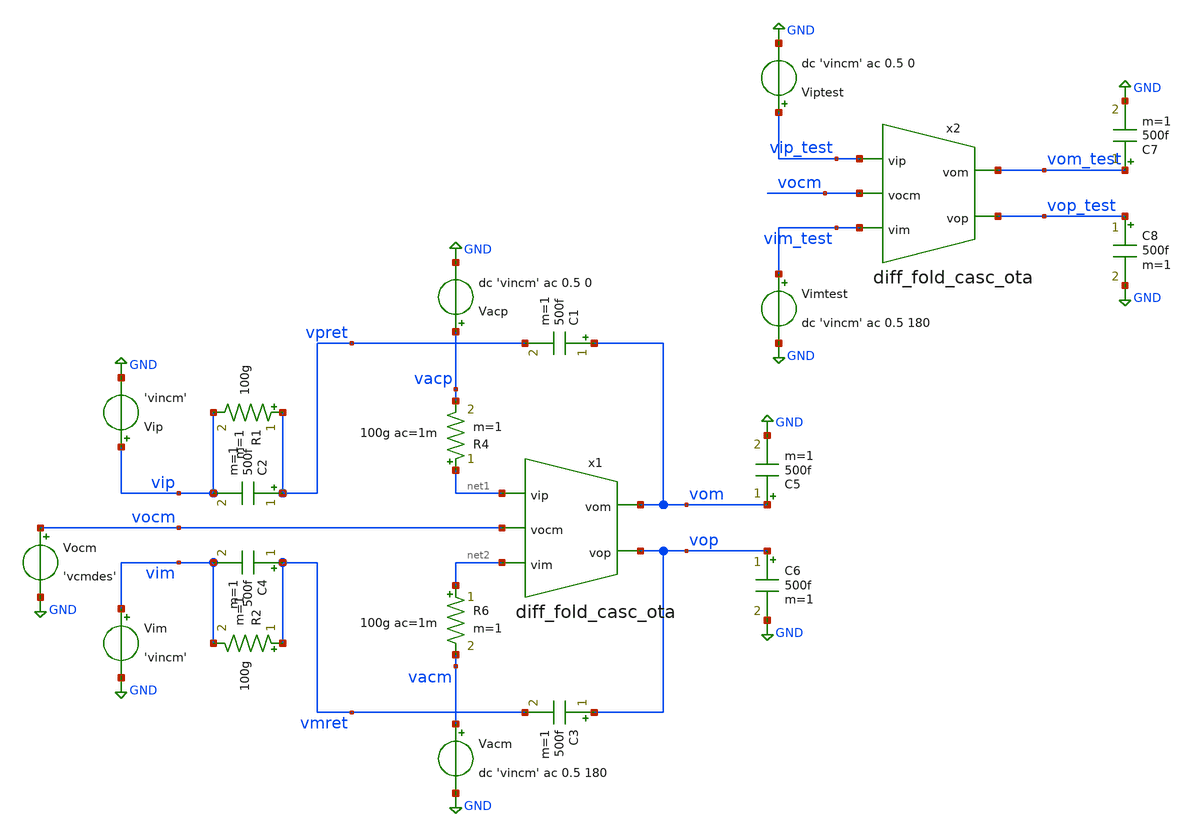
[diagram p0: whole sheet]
** sch_path: designs/diff_ota_stability_tb.sch
* Copyright 2020 Stefan Frederik Schippers
* Licensed under the Apache License, Version 2.0 (the "License");
* you may not use this file except in compliance with the License.
* You may obtain a copy of the License at
* https://www.apache.org/licenses/LICENSE-2.0
* Unless required by applicable law or agreed to in writing, software
* distributed under the License is distributed on an "AS IS" BASIS,
* WITHOUT WARRANTIES OR CONDITIONS OF ANY KIND, either express or implied.
* See the License for the specific language governing permissions and
* limitations under the License.
**.subckt diff_ota_stability_tb
C1 vom vpret 500f m=1
C2 vpret vip 500f m=1
C3 vop vmret 500f m=1
C4 vmret vim 500f m=1
C5 vom GND 500f m=1
C6 vop GND 500f m=1
R1 vpret vip 100g m=1
R2 vmret vim 100g m=1
R4 net1 vacp 100g ac=1m m=1
R6 net2 vacm 100g ac=1m m=1
Vacm vacm GND dc 'vincm' ac 0.5 180
Vacp vacp GND dc 'vincm' ac 0.5 0
Vip vip GND 'vincm'
Vim vim GND 'vincm'
Vocm vocm GND 'vcmdes'
Viptest vip_test GND dc 'vincm' ac 0.5 0
Vimtest vim_test GND dc 'vincm' ac 0.5 180
C7 vom_test GND 500f m=1
C8 vop_test GND 500f m=1
x1 vom vop net1 net2 vocm diff_fold_casc_ota Lbias=4.8 Ibias=10u Itail=10u Ccomp=2p
x2 vom_test vop_test vip_test vim_test vocm diff_fold_casc_ota Lbias=4.8 Ibias=10u Itail=10u
+ Ccomp=2p
**** begin user architecture code

.include $::SKYWATER_MODELS/cells/nfet_01v8/sky130_fd_pr__nfet_01v8__tt.corner.spice
.include $::SKYWATER_MODELS/cells/nfet_01v8_lvt/sky130_fd_pr__nfet_01v8_lvt__tt.corner.spice
.include $::SKYWATER_MODELS/cells/pfet_01v8/sky130_fd_pr__pfet_01v8__tt.corner.spice
.include $::SKYWATER_MODELS/cells/nfet_03v3_nvt/sky130_fd_pr__nfet_03v3_nvt__tt.corner.spice
.include $::SKYWATER_MODELS/cells/nfet_05v0_nvt/sky130_fd_pr__nfet_05v0_nvt__tt.corner.spice
.include $::SKYWATER_MODELS/cells/esd_nfet_01v8/sky130_fd_pr__esd_nfet_01v8__tt.corner.spice
.include $::SKYWATER_MODELS/cells/pfet_01v8_lvt/sky130_fd_pr__pfet_01v8_lvt__tt.corner.spice
.include $::SKYWATER_MODELS/cells/pfet_01v8_hvt/sky130_fd_pr__pfet_01v8_hvt__tt.corner.spice
.include $::SKYWATER_MODELS/cells/esd_pfet_g5v0d10v5/sky130_fd_pr__esd_pfet_g5v0d10v5__tt.corner.spice
.include $::SKYWATER_MODELS/cells/pfet_g5v0d10v5/sky130_fd_pr__pfet_g5v0d10v5__tt.corner.spice
.include $::SKYWATER_MODELS/cells/pfet_g5v0d16v0/sky130_fd_pr__pfet_g5v0d16v0__tt.corner.spice
.include $::SKYWATER_MODELS/cells/nfet_g5v0d10v5/sky130_fd_pr__nfet_g5v0d10v5__tt.corner.spice
.include $::SKYWATER_MODELS/cells/nfet_g5v0d16v0/sky130_fd_pr__nfet_g5v0d16v0__tt_discrete.corner.spice
.include $::SKYWATER_MODELS/cells/esd_nfet_g5v0d10v5/sky130_fd_pr__esd_nfet_g5v0d10v5__tt.corner.spice
.include $::SKYWATER_MODELS/models/corners/tt/nonfet.spice
* Mismatch parameters
.include $::SKYWATER_MODELS/cells/nfet_01v8/sky130_fd_pr__nfet_01v8__mismatch.corner.spice
.include $::SKYWATER_MODELS/cells/pfet_01v8/sky130_fd_pr__pfet_01v8__mismatch.corner.spice
.include $::SKYWATER_MODELS/cells/nfet_01v8_lvt/sky130_fd_pr__nfet_01v8_lvt__mismatch.corner.spice
.include $::SKYWATER_MODELS/cells/pfet_01v8_lvt/sky130_fd_pr__pfet_01v8_lvt__mismatch.corner.spice
.include $::SKYWATER_MODELS/cells/pfet_01v8_hvt/sky130_fd_pr__pfet_01v8_hvt__mismatch.corner.spice
.include $::SKYWATER_MODELS/cells/nfet_g5v0d10v5/sky130_fd_pr__nfet_g5v0d10v5__mismatch.corner.spice
.include $::SKYWATER_MODELS/cells/pfet_g5v0d10v5/sky130_fd_pr__pfet_g5v0d10v5__mismatch.corner.spice
.include $::SKYWATER_MODELS/cells/nfet_05v0_nvt/sky130_fd_pr__nfet_05v0_nvt__mismatch.corner.spice
.include $::SKYWATER_MODELS/cells/nfet_03v3_nvt/sky130_fd_pr__nfet_03v3_nvt__mismatch.corner.spice
* Resistor$::SKYWATER_MODELS/Capacitor
.include $::SKYWATER_MODELS/models/r+c/res_typical__cap_typical.spice
.include $::SKYWATER_MODELS/models/r+c/res_typical__cap_typical__lin.spice
* Special cells
.include $::SKYWATER_MODELS/models/corners/tt/specialized_cells.spice
* All models
.include $::SKYWATER_MODELS/models/all.spice
* Corner
.include $::SKYWATER_MODELS/models/corners/tt/rf.spice

**** end user architecture code
**.ends

* expanding   symbol:
*+  /home/users/nhpoole/ee272b/ee272b_mixed_signal_mmwave_accelerator/designs/diff_fold_casc_ota.sym # of pins=5
** sym_path: designs/diff_fold_casc_ota.sym
** sch_path: designs/diff_fold_casc_ota.sch
.subckt diff_fold_casc_ota vom vop vip vim vocm  Lbias=4.8 Ibias=10u Itail=10u Ccomp=2p
*.opin vop
*.opin vom
*.ipin vip
*.ipin vim
*.ipin vocm
V6 vtail_casc net1 0
XM7 net1 vbias4 GND GND sky130_fd_pr__nfet_01v8 L='Lbias*nfactorL' W='Wbias*nfactorW' nf=1 ad='int((nf+1)/2) * W/nf * 0.29'
+ as='int((nf+2)/2) * W/nf * 0.29' pd='2*int((nf+1)/2) * (W/nf + 0.29)' ps='2*int((nf+2)/2) * (W/nf + 0.29)'
+ nrd='0.29 / W' nrs='0.29 / W' sa=0 sb=0 sd=0 mult='9*K' m='9*K'
XM10 vcascnp vbias4 GND GND sky130_fd_pr__nfet_01v8 L='Lbias*nfactorL' W='Wbias*nfactorW' nf=1 ad='int((nf+1)/2) * W/nf * 0.29'
+ as='int((nf+2)/2) * W/nf * 0.29' pd='2*int((nf+1)/2) * (W/nf + 0.29)' ps='2*int((nf+2)/2) * (W/nf + 0.29)'
+ nrd='0.29 / W' nrs='0.29 / W' sa=0 sb=0 sd=0 mult='9*K' m='9*K'
XM11 vom vbias3 vcascnp GND sky130_fd_pr__nfet_01v8 L='Lbias*nfactorL' W='Wbias*nfactorW' nf=1 ad='int((nf+1)/2) * W/nf * 0.29'
+ as='int((nf+2)/2) * W/nf * 0.29' pd='2*int((nf+1)/2) * (W/nf + 0.29)' ps='2*int((nf+2)/2) * (W/nf + 0.29)'
+ nrd='0.29 / W' nrs='0.29 / W' sa=0 sb=0 sd=0 mult='9*K' m='9*K'
XM27 vcascnm vbias4 GND GND sky130_fd_pr__nfet_01v8 L='Lbias*nfactorL' W='Wbias*nfactorW' nf=1 ad='int((nf+1)/2) * W/nf * 0.29'
+ as='int((nf+2)/2) * W/nf * 0.29' pd='2*int((nf+1)/2) * (W/nf + 0.29)' ps='2*int((nf+2)/2) * (W/nf + 0.29)'
+ nrd='0.29 / W' nrs='0.29 / W' sa=0 sb=0 sd=0 mult='9*K' m='9*K'
XM28 vop vbias3 vcascnm GND sky130_fd_pr__nfet_01v8 L='Lbias*nfactorL' W='Wbias*nfactorW' nf=1 ad='int((nf+1)/2) * W/nf * 0.29'
+ as='int((nf+2)/2) * W/nf * 0.29' pd='2*int((nf+1)/2) * (W/nf + 0.29)' ps='2*int((nf+2)/2) * (W/nf + 0.29)'
+ nrd='0.29 / W' nrs='0.29 / W' sa=0 sb=0 sd=0 mult='9*K' m='9*K'
XM36 vbias1 vbias2 net7 VDD sky130_fd_pr__pfet_01v8 L='Lbias' W='2*Wbias' nf=1 ad='int((nf+1)/2) * W/nf * 0.29'
+ as='int((nf+2)/2) * W/nf * 0.29' pd='2*int((nf+1)/2) * (W/nf + 0.29)' ps='2*int((nf+2)/2) * (W/nf + 0.29)'
+ nrd='0.29 / W' nrs='0.29 / W' sa=0 sb=0 sd=0 mult='9*K' m='9*K'
XM37 net4 vbias2 net2 VDD sky130_fd_pr__pfet_01v8 L='Lbias' W='2*Wbias' nf=1 ad='int((nf+1)/2) * W/nf * 0.29'
+ as='int((nf+2)/2) * W/nf * 0.29' pd='2*int((nf+1)/2) * (W/nf + 0.29)' ps='2*int((nf+2)/2) * (W/nf + 0.29)'
+ nrd='0.29 / W' nrs='0.29 / W' sa=0 sb=0 sd=0 mult='9*K' m='9*K'
XM38 net6 vbias2 net5 VDD sky130_fd_pr__pfet_01v8 L='Lbias' W='2*Wbias' nf=1 ad='int((nf+1)/2) * W/nf * 0.29'
+ as='int((nf+2)/2) * W/nf * 0.29' pd='2*int((nf+1)/2) * (W/nf + 0.29)' ps='2*int((nf+2)/2) * (W/nf + 0.29)'
+ nrd='0.29 / W' nrs='0.29 / W' sa=0 sb=0 sd=0 mult='9*K' m='9*K'
XM39 vbias2 net3 vbias1 VDD sky130_fd_pr__pfet_01v8 L='Lbias' W='Wbias' nf=1 ad='int((nf+1)/2) * W/nf * 0.29'
+ as='int((nf+2)/2) * W/nf * 0.29' pd='2*int((nf+1)/2) * (W/nf + 0.29)' ps='2*int((nf+2)/2) * (W/nf + 0.29)'
+ nrd='0.29 / W' nrs='0.29 / W' sa=0 sb=0 sd=0 mult='3*K' m='3*K'
XM40 net3 net3 vbias2 VDD sky130_fd_pr__pfet_01v8 L='Lbias' W='3*Wbias' nf=1 ad='int((nf+1)/2) * W/nf * 0.29'
+ as='int((nf+2)/2) * W/nf * 0.29' pd='2*int((nf+1)/2) * (W/nf + 0.29)' ps='2*int((nf+2)/2) * (W/nf + 0.29)'
+ nrd='0.29 / W' nrs='0.29 / W' sa=0 sb=0 sd=0 mult='9*K' m='9*K'
XM41 net4 net4 vbias3 GND sky130_fd_pr__nfet_01v8 L='Lbias*nfactorL' W='3*Wbias*nfactorW' nf=1 ad='int((nf+1)/2) * W/nf * 0.29'
+ as='int((nf+2)/2) * W/nf * 0.29' pd='2*int((nf+1)/2) * (W/nf + 0.29)' ps='2*int((nf+2)/2) * (W/nf + 0.29)'
+ nrd='0.29 / W' nrs='0.29 / W' sa=0 sb=0 sd=0 mult='9*K' m='9*K'
XM42 vbias3 net4 vbias4 GND sky130_fd_pr__nfet_01v8 L='Lbias*nfactorL' W='Wbias*nfactorW' nf=1 ad='int((nf+1)/2) * W/nf * 0.29'
+ as='int((nf+2)/2) * W/nf * 0.29' pd='2*int((nf+1)/2) * (W/nf + 0.29)' ps='2*int((nf+2)/2) * (W/nf + 0.29)'
+ nrd='0.29 / W' nrs='0.29 / W' sa=0 sb=0 sd=0 mult='K' m='K'
XM43 vbias4 vbias3 net9 GND sky130_fd_pr__nfet_01v8 L='Lbias*nfactorL' W='Wbias*nfactorW' nf=1 ad='int((nf+1)/2) * W/nf * 0.29'
+ as='int((nf+2)/2) * W/nf * 0.29' pd='2*int((nf+1)/2) * (W/nf + 0.29)' ps='2*int((nf+2)/2) * (W/nf + 0.29)'
+ nrd='0.29 / W' nrs='0.29 / W' sa=0 sb=0 sd=0 mult='9*K' m='9*K'
XM44 net10 vbias4 GND GND sky130_fd_pr__nfet_01v8 L='Lbias*nfactorL' W='Wbias*nfactorW' nf=1 ad='int((nf+1)/2) * W/nf * 0.29'
+ as='int((nf+2)/2) * W/nf * 0.29' pd='2*int((nf+1)/2) * (W/nf + 0.29)' ps='2*int((nf+2)/2) * (W/nf + 0.29)'
+ nrd='0.29 / W' nrs='0.29 / W' sa=0 sb=0 sd=0 mult='9*K' m='9*K'
XM45 net6 net6 net8 net8 sky130_fd_pr__nfet_01v8 L='Lbias' W='0.6*Wbias' nf=1 ad='int((nf+1)/2) * W/nf * 0.29'
+ as='int((nf+2)/2) * W/nf * 0.29' pd='2*int((nf+1)/2) * (W/nf + 0.29)' ps='2*int((nf+2)/2) * (W/nf + 0.29)'
+ nrd='0.29 / W' nrs='0.29 / W' sa=0 sb=0 sd=0 mult='K' m='K'
I1 net3 GND 'Ibias'
V7 net8 GND 0
V8 net9 net10 0
XM46 vcmn_casc_tail1 vnbiascm_casc GND GND sky130_fd_pr__nfet_01v8 L=1.2 W=0.7 nf=1 ad='int((nf+1)/2) * W/nf * 0.29'
+ as='int((nf+2)/2) * W/nf * 0.29' pd='2*int((nf+1)/2) * (W/nf + 0.29)' ps='2*int((nf+2)/2) * (W/nf + 0.29)'
+ nrd='0.29 / W' nrs='0.29 / W' sa=0 sb=0 sd=0 mult=1 m=1
XM47 vcmn_casc_tail2 vnbiascm_casc GND GND sky130_fd_pr__nfet_01v8 L=1.2 W=0.7 nf=1 ad='int((nf+1)/2) * W/nf * 0.29'
+ as='int((nf+2)/2) * W/nf * 0.29' pd='2*int((nf+1)/2) * (W/nf + 0.29)' ps='2*int((nf+2)/2) * (W/nf + 0.29)'
+ nrd='0.29 / W' nrs='0.29 / W' sa=0 sb=0 sd=0 mult=1 m=1
XM48 vcmcn2_casc vcmcn2_casc VDD VDD sky130_fd_pr__pfet_01v8 L=0.8 W='Wp' nf=1 ad='int((nf+1)/2) * W/nf * 0.29'
+ as='int((nf+2)/2) * W/nf * 0.29' pd='2*int((nf+1)/2) * (W/nf + 0.29)' ps='2*int((nf+2)/2) * (W/nf + 0.29)'
+ nrd='0.29 / W' nrs='0.29 / W' sa=0 sb=0 sd=0 mult=1 m=1
XM49 vcmcn_casc vcmcn_casc VDD VDD sky130_fd_pr__pfet_01v8 L=0.8 W='Wp' nf=1 ad='int((nf+1)/2) * W/nf * 0.29'
+ as='int((nf+2)/2) * W/nf * 0.29' pd='2*int((nf+1)/2) * (W/nf + 0.29)' ps='2*int((nf+2)/2) * (W/nf + 0.29)'
+ nrd='0.29 / W' nrs='0.29 / W' sa=0 sb=0 sd=0 mult=1 m=1
I4 VDD vnbiascm_casc 'Itail'
XM50 vnbiascm_casc vnbiascm_casc GND GND sky130_fd_pr__nfet_01v8 L=1.2 W=0.7 nf=1 ad='int((nf+1)/2) * W/nf * 0.29'
+ as='int((nf+2)/2) * W/nf * 0.29' pd='2*int((nf+1)/2) * (W/nf + 0.29)' ps='2*int((nf+2)/2) * (W/nf + 0.29)'
+ nrd='0.29 / W' nrs='0.29 / W' sa=0 sb=0 sd=0 mult=1 m=1
XM51 vcmcn_casc vop vcmn_casc_tail1 GND sky130_fd_pr__nfet_01v8_lvt L=0.3 W='Wncm' nf=1 ad='int((nf+1)/2) * W/nf * 0.29'
+ as='int((nf+2)/2) * W/nf * 0.29' pd='2*int((nf+1)/2) * (W/nf + 0.29)' ps='2*int((nf+2)/2) * (W/nf + 0.29)'
+ nrd='0.29 / W' nrs='0.29 / W' sa=0 sb=0 sd=0 mult=1 m=1
XM52 vcmcn1_casc vocm vcmn_casc_tail1 GND sky130_fd_pr__nfet_01v8_lvt L=0.3 W='Wncm' nf=1 ad='int((nf+1)/2) * W/nf * 0.29'
+ as='int((nf+2)/2) * W/nf * 0.29' pd='2*int((nf+1)/2) * (W/nf + 0.29)' ps='2*int((nf+2)/2) * (W/nf + 0.29)'
+ nrd='0.29 / W' nrs='0.29 / W' sa=0 sb=0 sd=0 mult=1 m=1
XM53 vcmcn_casc vom vcmn_casc_tail2 GND sky130_fd_pr__nfet_01v8_lvt L=0.3 W='Wncm' nf=1 ad='int((nf+1)/2) * W/nf * 0.29'
+ as='int((nf+2)/2) * W/nf * 0.29' pd='2*int((nf+1)/2) * (W/nf + 0.29)' ps='2*int((nf+2)/2) * (W/nf + 0.29)'
+ nrd='0.29 / W' nrs='0.29 / W' sa=0 sb=0 sd=0 mult=1 m=1
XM54 vcmcn2_casc vocm vcmn_casc_tail2 GND sky130_fd_pr__nfet_01v8_lvt L=0.3 W='Wncm' nf=1 ad='int((nf+1)/2) * W/nf * 0.29'
+ as='int((nf+2)/2) * W/nf * 0.29' pd='2*int((nf+1)/2) * (W/nf + 0.29)' ps='2*int((nf+2)/2) * (W/nf + 0.29)'
+ nrd='0.29 / W' nrs='0.29 / W' sa=0 sb=0 sd=0 mult=1 m=1
XM56 net11 vcmcn_casc VDD VDD sky130_fd_pr__pfet_01v8 L=0.8 W='Wp' nf=1 ad='int((nf+1)/2) * W/nf * 0.29'
+ as='int((nf+2)/2) * W/nf * 0.29' pd='2*int((nf+1)/2) * (W/nf + 0.29)' ps='2*int((nf+2)/2) * (W/nf + 0.29)'
+ nrd='0.29 / W' nrs='0.29 / W' sa=0 sb=0 sd=0 mult=1 m=1
XM57 vcmcn1_casc vcmcn1_casc VDD VDD sky130_fd_pr__pfet_01v8 L=0.8 W='Wp' nf=1 ad='int((nf+1)/2) * W/nf * 0.29'
+ as='int((nf+2)/2) * W/nf * 0.29' pd='2*int((nf+1)/2) * (W/nf + 0.29)' ps='2*int((nf+2)/2) * (W/nf + 0.29)'
+ nrd='0.29 / W' nrs='0.29 / W' sa=0 sb=0 sd=0 mult=1 m=1
V11 net11 vcmc_casc 0
XM12 vom vbias2 vfoldp VDD sky130_fd_pr__pfet_01v8 L='Lbias' W='2*Wbias' nf=1 ad='int((nf+1)/2) * W/nf * 0.29'
+ as='int((nf+2)/2) * W/nf * 0.29' pd='2*int((nf+1)/2) * (W/nf + 0.29)' ps='2*int((nf+2)/2) * (W/nf + 0.29)'
+ nrd='0.29 / W' nrs='0.29 / W' sa=0 sb=0 sd=0 mult='9*K' m='9*K'
XM31 vop vbias2 vfoldm VDD sky130_fd_pr__pfet_01v8 L='Lbias' W='2*Wbias' nf=1 ad='int((nf+1)/2) * W/nf * 0.29'
+ as='int((nf+2)/2) * W/nf * 0.29' pd='2*int((nf+1)/2) * (W/nf + 0.29)' ps='2*int((nf+2)/2) * (W/nf + 0.29)'
+ nrd='0.29 / W' nrs='0.29 / W' sa=0 sb=0 sd=0 mult='9*K' m='9*K'
XM15 vfoldp vbias1 VDD VDD sky130_fd_pr__pfet_01v8_lvt L='Lbias' W='4*Wbias' nf=1 ad='int((nf+1)/2) * W/nf * 0.29'
+ as='int((nf+2)/2) * W/nf * 0.29' pd='2*int((nf+1)/2) * (W/nf + 0.29)' ps='2*int((nf+2)/2) * (W/nf + 0.29)'
+ nrd='0.29 / W' nrs='0.29 / W' sa=0 sb=0 sd=0 mult='9*K' m='9*K'
XM32 vfoldm vbias1 VDD VDD sky130_fd_pr__pfet_01v8_lvt L='Lbias' W='4*Wbias' nf=1 ad='int((nf+1)/2) * W/nf * 0.29'
+ as='int((nf+2)/2) * W/nf * 0.29' pd='2*int((nf+1)/2) * (W/nf + 0.29)' ps='2*int((nf+2)/2) * (W/nf + 0.29)'
+ nrd='0.29 / W' nrs='0.29 / W' sa=0 sb=0 sd=0 mult='9*K' m='9*K'
XM33 net7 vbias1 VDD VDD sky130_fd_pr__pfet_01v8_lvt L='Lbias' W='2*Wbias' nf=1 ad='int((nf+1)/2) * W/nf * 0.29'
+ as='int((nf+2)/2) * W/nf * 0.29' pd='2*int((nf+1)/2) * (W/nf + 0.29)' ps='2*int((nf+2)/2) * (W/nf + 0.29)'
+ nrd='0.29 / W' nrs='0.29 / W' sa=0 sb=0 sd=0 mult='9*K' m='9*K'
XM34 net2 vbias1 VDD VDD sky130_fd_pr__pfet_01v8_lvt L='Lbias' W='2*Wbias' nf=1 ad='int((nf+1)/2) * W/nf * 0.29'
+ as='int((nf+2)/2) * W/nf * 0.29' pd='2*int((nf+1)/2) * (W/nf + 0.29)' ps='2*int((nf+2)/2) * (W/nf + 0.29)'
+ nrd='0.29 / W' nrs='0.29 / W' sa=0 sb=0 sd=0 mult='9*K' m='9*K'
XM35 net5 vbias1 VDD VDD sky130_fd_pr__pfet_01v8_lvt L='Lbias' W='2*Wbias' nf=1 ad='int((nf+1)/2) * W/nf * 0.29'
+ as='int((nf+2)/2) * W/nf * 0.29' pd='2*int((nf+1)/2) * (W/nf + 0.29)' ps='2*int((nf+2)/2) * (W/nf + 0.29)'
+ nrd='0.29 / W' nrs='0.29 / W' sa=0 sb=0 sd=0 mult='9*K' m='9*K'
XM5 net1 vcmc_casc GND GND sky130_fd_pr__nfet_01v8 L='Lbias*nfactorL' W='Wbias*nfactorW' nf=1 ad='int((nf+1)/2) * W/nf * 0.29'
+ as='int((nf+2)/2) * W/nf * 0.29' pd='2*int((nf+1)/2) * (W/nf + 0.29)' ps='2*int((nf+2)/2) * (W/nf + 0.29)'
+ nrd='0.29 / W' nrs='0.29 / W' sa=0 sb=0 sd=0 mult='9*K' m='9*K'
XM55 vcmc_casc vcmc_casc GND GND sky130_fd_pr__nfet_01v8 L='Lbias*nfactorL' W='Wbias*nfactorW' nf=1 ad='int((nf+1)/2) * W/nf * 0.29'
+ as='int((nf+2)/2) * W/nf * 0.29' pd='2*int((nf+1)/2) * (W/nf + 0.29)' ps='2*int((nf+2)/2) * (W/nf + 0.29)'
+ nrd='0.29 / W' nrs='0.29 / W' sa=0 sb=0 sd=0 mult='9*K' m='9*K'
XM58 vfoldp vim vfoldp GND sky130_fd_pr__nfet_01v8 L='K2*Lbias*nfactorL' W='Wbias*nfactorW' nf=1 ad='int((nf+1)/2) * W/nf * 0.29'
+ as='int((nf+2)/2) * W/nf * 0.29' pd='2*int((nf+1)/2) * (W/nf + 0.29)' ps='2*int((nf+2)/2) * (W/nf + 0.29)'
+ nrd='0.29 / W' nrs='0.29 / W' sa=0 sb=0 sd=0 mult='9*K' m='9*K'
XM59 vfoldm vip vfoldm GND sky130_fd_pr__nfet_01v8 L='K2*Lbias*nfactorL' W='Wbias*nfactorW' nf=1 ad='int((nf+1)/2) * W/nf * 0.29'
+ as='int((nf+2)/2) * W/nf * 0.29' pd='2*int((nf+1)/2) * (W/nf + 0.29)' ps='2*int((nf+2)/2) * (W/nf + 0.29)'
+ nrd='0.29 / W' nrs='0.29 / W' sa=0 sb=0 sd=0 mult='9*K' m='9*K'
C1 vom GND 'Ccomp' m=1
C2 vop GND 'Ccomp' m=1
XM8 vfoldp vip vtail_casc GND sky130_fd_pr__nfet_01v8_lvt L='K2*Lbias*nfactorL' W='Wbias*nfactorW' nf=1
+ ad='int((nf+1)/2) * W/nf * 0.29' as='int((nf+2)/2) * W/nf * 0.29' pd='2*int((nf+1)/2) * (W/nf + 0.29)'
+ ps='2*int((nf+2)/2) * (W/nf + 0.29)' nrd='0.29 / W' nrs='0.29 / W' sa=0 sb=0 sd=0 mult='9*K' m='9*K'
XM9 vfoldm vim vtail_casc GND sky130_fd_pr__nfet_01v8_lvt L='K2*Lbias*nfactorL' W='Wbias*nfactorW' nf=1
+ ad='int((nf+1)/2) * W/nf * 0.29' as='int((nf+2)/2) * W/nf * 0.29' pd='2*int((nf+1)/2) * (W/nf + 0.29)'
+ ps='2*int((nf+2)/2) * (W/nf + 0.29)' nrd='0.29 / W' nrs='0.29 / W' sa=0 sb=0 sd=0 mult='9*K' m='9*K'
.ends

.GLOBAL GND
.GLOBAL VDD
**** begin user architecture code

.include diff_ota_stability_tb_commands.spice

**** end user architecture code
.end
